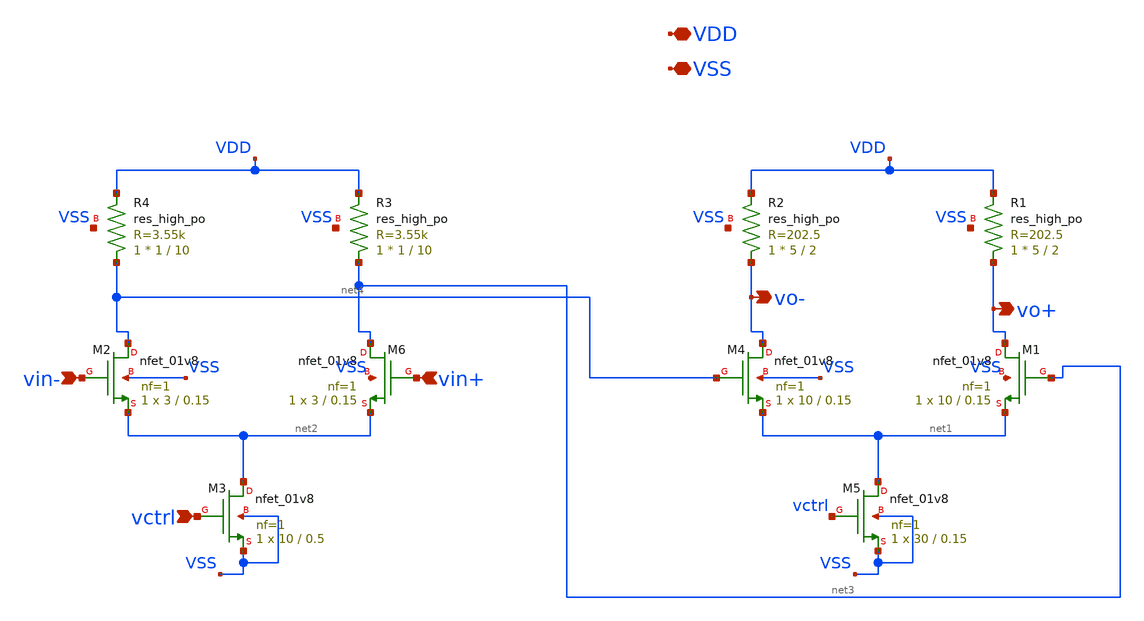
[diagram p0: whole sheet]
** sch_path: xschem/diff_savefile.sch
**.subckt diff_savefile VDD VSS vo+ vo- vin- vctrl vin+
*.iopin VDD
*.iopin VSS
*.opin vo+
*.opin vo-
*.ipin vin-
*.ipin vctrl
*.ipin vin+
XM4 vo- net4 net1 VSS sky130_fd_pr__nfet_01v8 L=0.15 W=10 nf=1 ad='int((nf+1)/2) * W/nf * 0.29' as='int((nf+2)/2) * W/nf * 0.29'
+ pd='2*int((nf+1)/2) * (W/nf + 0.29)' ps='2*int((nf+2)/2) * (W/nf + 0.29)' nrd='0.29 / W' nrs='0.29 / W'
+ sa=0 sb=0 sd=0 mult=1 m=1
XM5 net1 vctrl VSS VSS sky130_fd_pr__nfet_01v8 L=0.15 W=30 nf=1 ad='int((nf+1)/2) * W/nf * 0.29' as='int((nf+2)/2) * W/nf * 0.29'
+ pd='2*int((nf+1)/2) * (W/nf + 0.29)' ps='2*int((nf+2)/2) * (W/nf + 0.29)' nrd='0.29 / W' nrs='0.29 / W'
+ sa=0 sb=0 sd=0 mult=1 m=1
XM1 vo+ net3 net1 VSS sky130_fd_pr__nfet_01v8 L=0.15 W=10 nf=1 ad='int((nf+1)/2) * W/nf * 0.29' as='int((nf+2)/2) * W/nf * 0.29'
+ pd='2*int((nf+1)/2) * (W/nf + 0.29)' ps='2*int((nf+2)/2) * (W/nf + 0.29)' nrd='0.29 / W' nrs='0.29 / W'
+ sa=0 sb=0 sd=0 mult=1 m=1
XR1 vo+ VDD VSS sky130_fd_pr__res_high_po W=5 L=2 mult=1 m=1
XR2 vo- VDD VSS sky130_fd_pr__res_high_po W=5 L=2 mult=1 m=1
XM2 net4 vin- net2 VSS sky130_fd_pr__nfet_01v8 L=0.15 W=3 nf=1 ad='int((nf+1)/2) * W/nf * 0.29' as='int((nf+2)/2) * W/nf * 0.29'
+ pd='2*int((nf+1)/2) * (W/nf + 0.29)' ps='2*int((nf+2)/2) * (W/nf + 0.29)' nrd='0.29 / W' nrs='0.29 / W'
+ sa=0 sb=0 sd=0 mult=1 m=1
XM3 net2 vctrl VSS VSS sky130_fd_pr__nfet_01v8 L=0.5 W=10 nf=1 ad='int((nf+1)/2) * W/nf * 0.29' as='int((nf+2)/2) * W/nf * 0.29'
+ pd='2*int((nf+1)/2) * (W/nf + 0.29)' ps='2*int((nf+2)/2) * (W/nf + 0.29)' nrd='0.29 / W' nrs='0.29 / W'
+ sa=0 sb=0 sd=0 mult=1 m=1
XM6 net3 vin+ net2 VSS sky130_fd_pr__nfet_01v8 L=0.15 W=3 nf=1 ad='int((nf+1)/2) * W/nf * 0.29' as='int((nf+2)/2) * W/nf * 0.29'
+ pd='2*int((nf+1)/2) * (W/nf + 0.29)' ps='2*int((nf+2)/2) * (W/nf + 0.29)' nrd='0.29 / W' nrs='0.29 / W'
+ sa=0 sb=0 sd=0 mult=1 m=1
XR3 net3 VDD VSS sky130_fd_pr__res_high_po W=1 L=10 mult=1 m=1
XR4 net4 VDD VSS sky130_fd_pr__res_high_po W=1 L=10 mult=1 m=1
**.ends
.end
